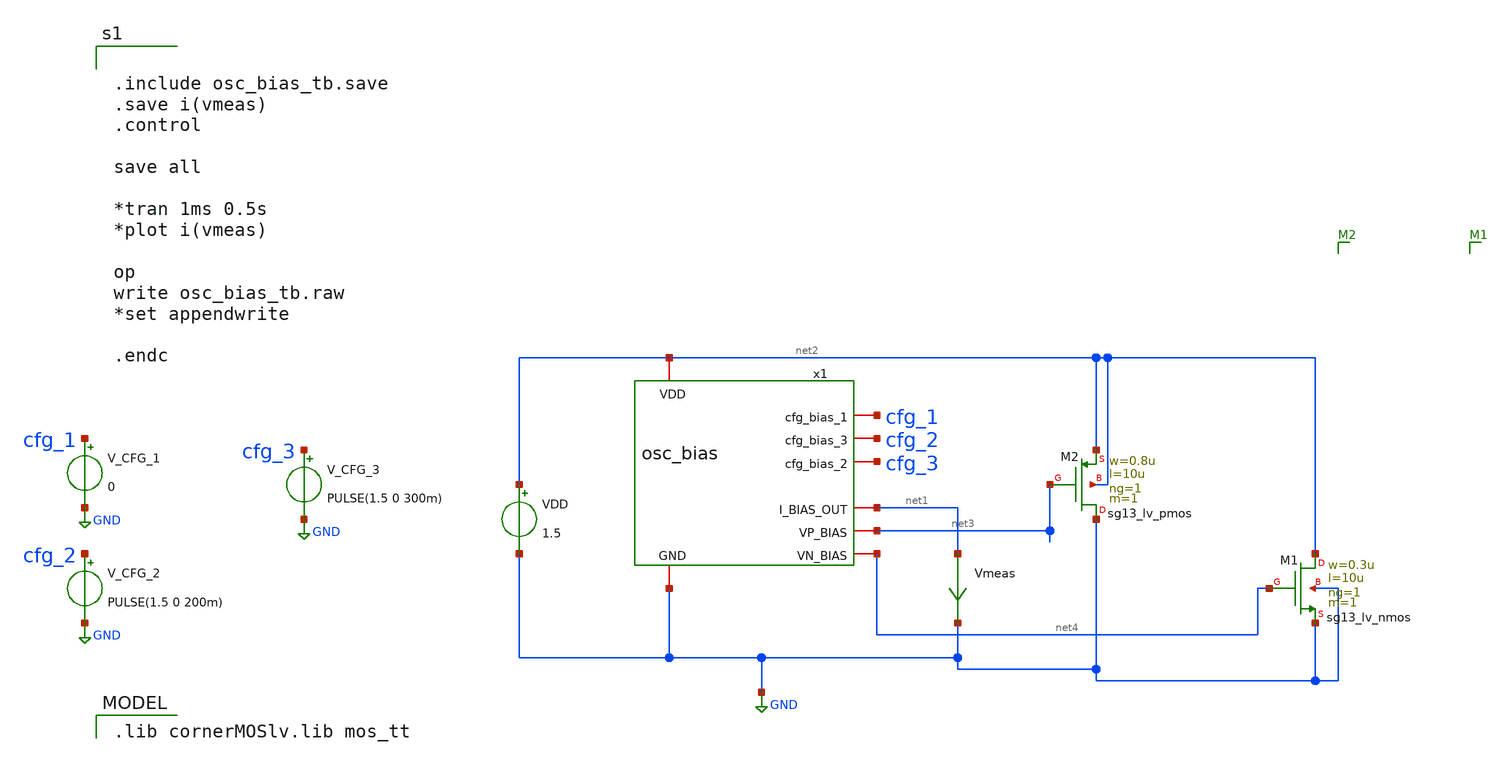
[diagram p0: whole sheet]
** sch_path: osc_bias_tb.sch
**.subckt osc_bias_tb
VDD net2 GND 1.5
Vmeas net1 GND 0
.save i(vmeas)
x1 net2 cfg_1 cfg_2 cfg_3 GND net1 net3 net4 osc_bias
V_CFG_1 cfg_1 GND 0
V_CFG_2 cfg_2 GND PULSE(1.5 0 200m)
V_CFG_3 cfg_3 GND PULSE(1.5 0 300m)
XM1 net2 net4 GND GND sg13_lv_nmos w=0.3u l=10u ng=1 m=1 mm_ok=1
XM2 GND net3 net2 net2 sg13_lv_pmos w=0.8u l=10u ng=1 m=1 mm_ok=1
**** begin user architecture code
 .lib cornerMOSlv.lib mos_tt



.include osc_bias_tb.save
.save i(vmeas)
.control

save all

*tran 1ms 0.5s
*plot i(vmeas)

op
write osc_bias_tb.raw
*set appendwrite

.endc


**** end user architecture code
**.ends

* expanding   symbol:  osc_bias.sym # of pins=8
** sym_path: osc_bias.sym
** sch_path: osc_bias.sch
.subckt osc_bias VDD cfg_bias_1 cfg_bias_3 cfg_bias_2 GND I_BIAS_OUT VP_BIAS VN_BIAS
*.iopin VDD
*.iopin GND
*.iopin I_BIAS_OUT
*.iopin cfg_bias_1
*.iopin cfg_bias_2
*.iopin cfg_bias_3
*.opin VN_BIAS
*.opin VP_BIAS
XM1 VP_BIAS VP_BIAS VDD VDD sg13_lv_pmos w=0.25u l=10u ng=1 m=1 mm_ok=1
XM3 VP_BIAS VP_BIAS net1 GND sg13_lv_nmos w=0.25u l=10u ng=1 m=1 mm_ok=1
XM4 net1 net1 net2 GND sg13_lv_nmos w=0.25u l=10u ng=1 m=1 mm_ok=1
XM5 net2 net2 net7 GND sg13_lv_nmos w=0.25u l=10u ng=1 m=1 mm_ok=1
XM2 net6 VP_BIAS VDD VDD sg13_lv_pmos w=2u l=10u ng=1 m=1 mm_ok=1
XM6 I_BIAS_OUT cfg_bias_1 net6 VDD sg13_lv_pmos w=0.25u l=10u ng=1 m=1 mm_ok=1
XM7 net3 VP_BIAS VDD VDD sg13_lv_pmos w=0.5u l=10u ng=1 m=1 mm_ok=1
XM8 net4 VP_BIAS VDD VDD sg13_lv_pmos w=1u l=10u ng=1 m=1 mm_ok=1
XM9 I_BIAS_OUT cfg_bias_2 net3 VDD sg13_lv_pmos w=0.5u l=10u ng=1 m=1 mm_ok=1
XM10 I_BIAS_OUT cfg_bias_3 net4 VDD sg13_lv_pmos w=1u l=10u ng=1 m=1 mm_ok=1
XM11 VN_BIAS VN_BIAS net5 GND sg13_lv_nmos w=0.25u l=10u ng=1 m=1 mm_ok=1
Vmeas net5 GND 0
.save i(vmeas)
C1 VDD VP_BIAS 1p m=1
R1 VDD VP_BIAS 100Meg m=1
XM12 net7 net7 VN_BIAS GND sg13_lv_nmos w=0.25u l=10u ng=1 m=1 mm_ok=1
.ends

.GLOBAL GND
.end
